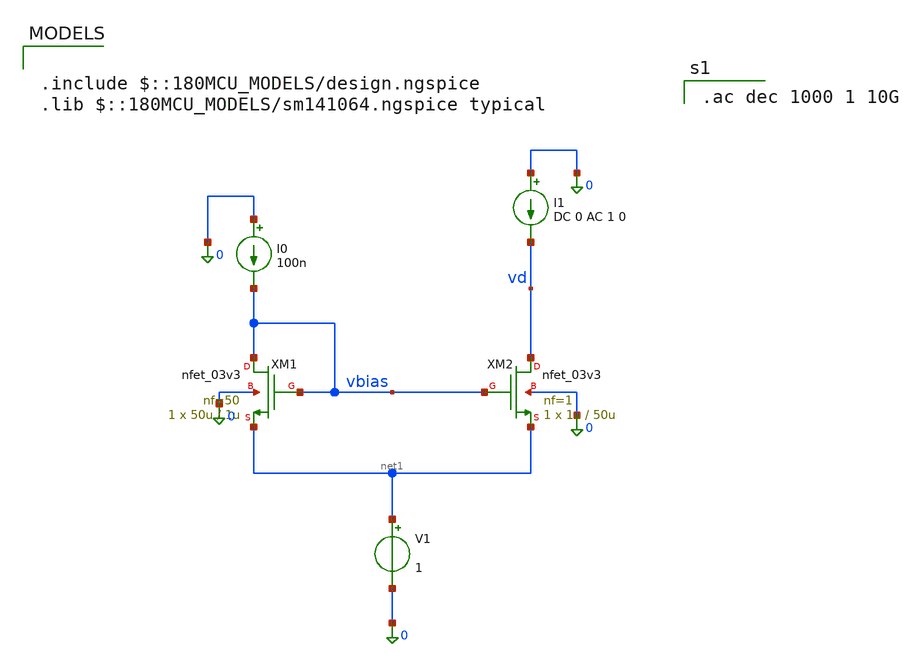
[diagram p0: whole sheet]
** sch_path: xschem/archive/pseudores/pseudores_test.sch
**.subckt pseudores_test
XM1 vbias vbias net1 0 nfet_03v3 L=1u W=50u nf=50 ad='int((nf+1)/2) * W/nf * 0.18u' as='int((nf+2)/2) * W/nf * 0.18u'
+ pd='2*int((nf+1)/2) * (W/nf + 0.18u)' ps='2*int((nf+2)/2) * (W/nf + 0.18u)' nrd='0.18u / W' nrs='0.18u / W'
+ sa=0 sb=0 sd=0 m=1
XM2 vd vbias net1 0 nfet_03v3 L=50u W=1u nf=1 ad='int((nf+1)/2) * W/nf * 0.18u' as='int((nf+2)/2) * W/nf * 0.18u'
+ pd='2*int((nf+1)/2) * (W/nf + 0.18u)' ps='2*int((nf+2)/2) * (W/nf + 0.18u)' nrd='0.18u / W' nrs='0.18u / W'
+ sa=0 sb=0 sd=0 m=1
I0 0 vbias 100n
I1 0 vd DC 0 AC 1 0
V1 net1 0 1
**** begin user architecture code

.include $::180MCU_MODELS/design.ngspice
.lib $::180MCU_MODELS/sm141064.ngspice typical


.ac dec 1000 1 10G

**** end user architecture code
**.ends
.end
